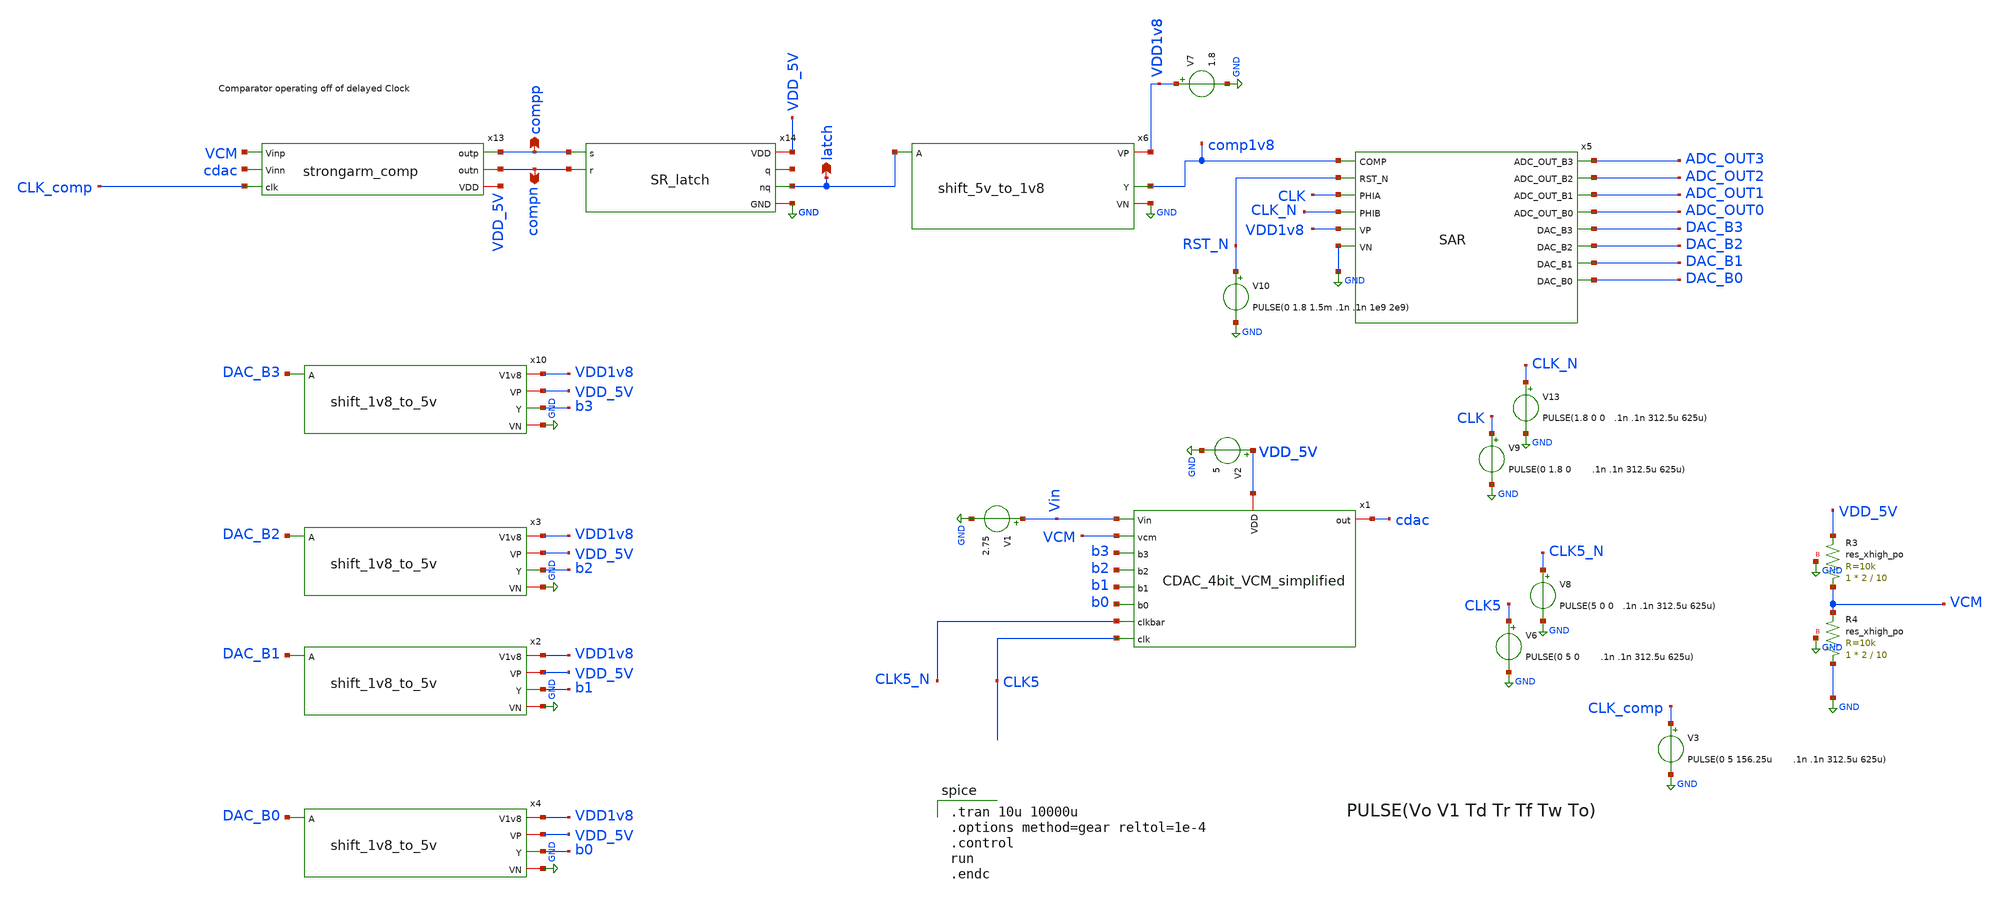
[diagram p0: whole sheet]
** sch_path: ADC/16bit_C2C/MagicAndSpice/CDAC_4bit_VCM_simplified_TB_inverter_test2_apr19_clkdelaycomp_invimprove.sch
**.subckt CDAC_4bit_VCM_simplified_TB_inverter_test2_apr19_clkdelaycomp_invimprove compp latch compn
*.opin compp
*.opin latch
*.opin compn
V2 VDD_5V GND 5
V1 Vin GND 2.75
x1 CLK5_N CLK5 Vin b3 b0 b2 b1 VCM cdac VDD_5V CDAC_4bit_VCM_simplified
V7 VDD1v8 GND 1.8
x6 VDD1v8 latch comp1v8 GND shift_5v_to_1v8
V10 RST_N GND PULSE(0 1.8 1.5m .1n .1n 1e9 2e9)
x13 compp compn VCM cdac VDD_5V CLK_comp strongarm_comp
x14 VDD_5V net1 compp latch compn GND SR_latch
V6 CLK5 GND PULSE(0 5 0 .1n .1n 312.5u 625u)
V8 CLK5_N GND PULSE(5 0 0 .1n .1n 312.5u 625u)
V9 CLK GND PULSE(0 1.8 0 .1n .1n 312.5u 625u)
V13 CLK_N GND PULSE(1.8 0 0 .1n .1n 312.5u 625u)
V3 CLK_comp GND PULSE(0 5 156.25u .1n .1n 312.5u 625u)
x10 VDD1v8 VDD_5V DAC_B3 b3 GND shift_1v8_to_5v
x3 VDD1v8 VDD_5V DAC_B2 b2 GND shift_1v8_to_5v
x2 VDD1v8 VDD_5V DAC_B1 b1 GND shift_1v8_to_5v
x4 VDD1v8 VDD_5V DAC_B0 b0 GND shift_1v8_to_5v
x5 comp1v8 RST_N CLK CLK_N ADC_OUT3 ADC_OUT2 ADC_OUT1 ADC_OUT0 DAC_B3 DAC_B2 DAC_B1 DAC_B0 VDD1v8
+ GND SAR
XR3 VCM VDD_5V GND sky130_fd_pr__res_xhigh_po W=2 L=10 mult=1 m=1
XR4 GND VCM GND sky130_fd_pr__res_xhigh_po W=2 L=10 mult=1 m=1
**** begin user architecture code

** opencircuitdesign pdks install
.lib $::SKYWATER_MODELS/sky130.lib.spice tt



.tran 10u 10000u
.options method=gear reltol=1e-4
.control
run
.endc

**** end user architecture code
**.ends
.GLOBAL GND
.end
